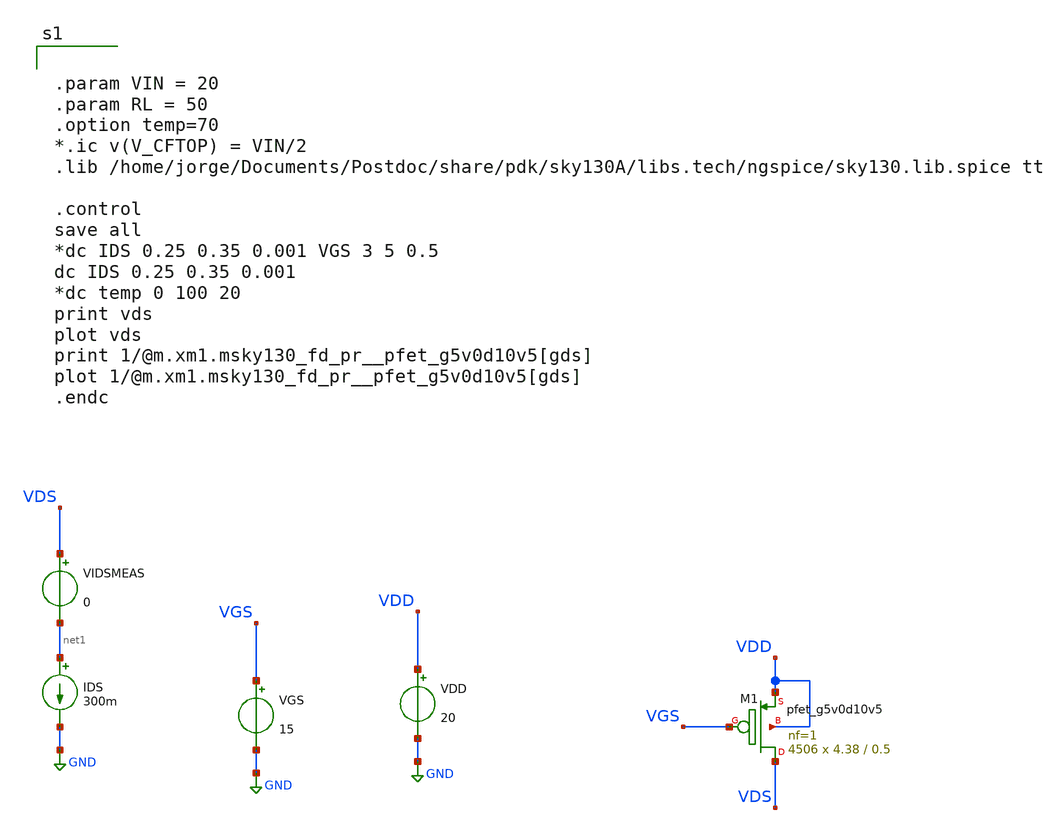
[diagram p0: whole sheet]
** sch_path: xschem/dev_switches/PMOS_allfingers_RONcalc_v2p2_20220623.sch
**.subckt PMOS_allfingers_RONcalc_v2p2_20220623
VGS VGS GND 15
IDS net1 GND 300m
VIDSMEAS VDS net1 0
XM1 VDS VGS VDD VDD sky130_fd_pr__pfet_g5v0d10v5 L=0.5 W=4.38 nf=1 ad='int((nf+1)/2) * W/nf * 0.29' as='int((nf+2)/2) * W/nf * 0.29'
+ pd='2*int((nf+1)/2) * (W/nf + 0.29)' ps='2*int((nf+2)/2) * (W/nf + 0.29)' nrd='0.29 / W' nrs='0.29 / W'
+ sa=0 sb=0 sd=0 mult=4506 m=4506
VDD VDD GND 20
**** begin user architecture code


.param VIN = 20
.param RL = 50
.option temp=70
*.ic v(V_CFTOP) = VIN/2
.lib /home/jorge/Documents/Postdoc/share/pdk/sky130A/libs.tech/ngspice/sky130.lib.spice tt

.control
save all
*dc IDS 0.25 0.35 0.001 VGS 3 5 0.5
dc IDS 0.25 0.35 0.001
*dc temp 0 100 20
print vds
plot vds
print 1/@m.xm1.msky130_fd_pr__pfet_g5v0d10v5[gds]
plot 1/@m.xm1.msky130_fd_pr__pfet_g5v0d10v5[gds]
.endc


**** end user architecture code
**.ends
.GLOBAL GND
.end
